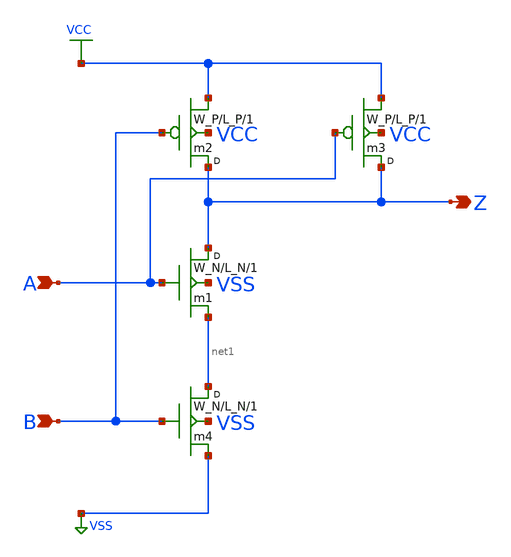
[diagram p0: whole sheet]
** sch_path: xschem_library/examples/nand2.sch
**.subckt nand2 A Z B
*.ipin A
*.opin Z
*.ipin B
m1 Z A net1 VSS CMOSN w=W_N l=L_N m=1
m4 net1 B VSS VSS CMOSN w=W_N l=L_N m=1
m2 Z B VCC VCC CMOSP w=W_P l=L_P m=1
m3 Z A VCC VCC CMOSP w=W_P l=L_P m=1
**.ends
.GLOBAL VSS
.GLOBAL VCC
.end
